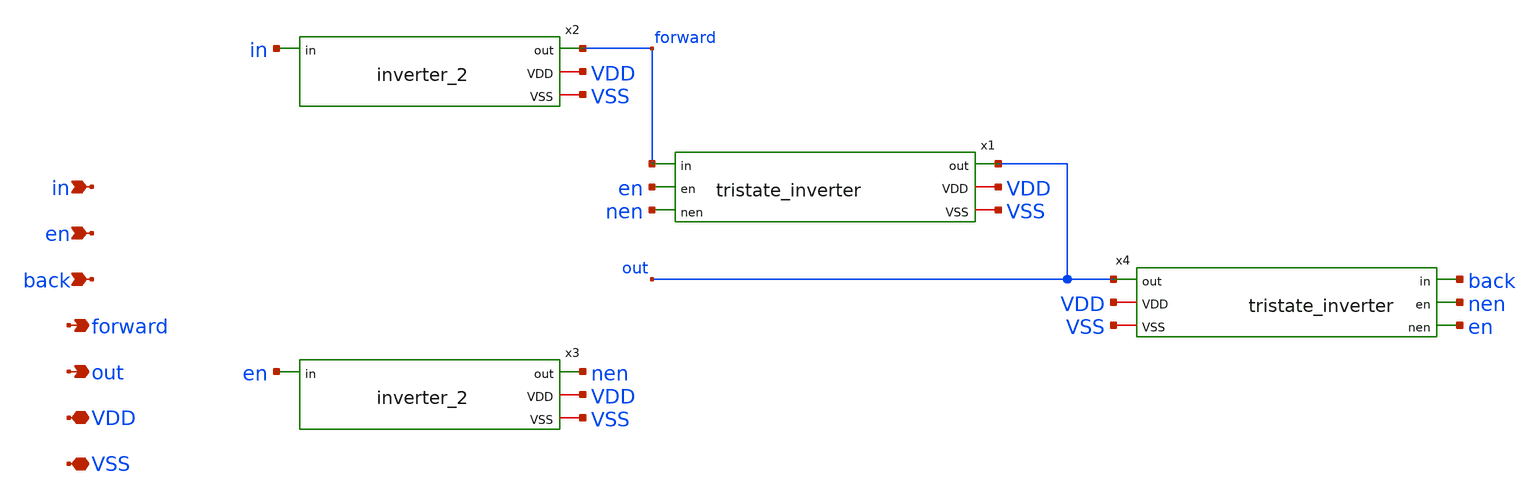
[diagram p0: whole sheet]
** sch_path: xschem/variable_delay_unit.sch
**.subckt variable_delay_unit VDD in out VSS en back forward
*.iopin VDD
*.ipin in
*.opin out
*.iopin VSS
*.ipin en
*.ipin back
*.opin forward
x1 forward en nen out VDD VSS tristate_inverter
x2 in forward VDD VSS inverter_2
x3 en nen VDD VSS inverter_2
x4 back nen en out VDD VSS tristate_inverter
**.ends

* expanding   symbol:  tristate_inverter.sym # of pins=6
** sym_path: xschem/tristate_inverter.sym
** sch_path: xschem/tristate_inverter.sch
.subckt tristate_inverter in en nen out VDD VSS
*.iopin VDD
*.ipin in
*.opin out
*.iopin VSS
*.ipin en
*.ipin nen
XM5 out in net2 VDD sky130_fd_pr__pfet_01v8 L=0.15 W=3 nf=1 ad='int((nf+1)/2) * W/nf * 0.29' as='int((nf+2)/2) * W/nf * 0.29'
+ pd='2*int((nf+1)/2) * (W/nf + 0.29)' ps='2*int((nf+2)/2) * (W/nf + 0.29)' nrd='0.29 / W' nrs='0.29 / W'
+ sa=0 sb=0 sd=0 mult=1 m=1
XM7 out in net1 VSS sky130_fd_pr__nfet_01v8 L=0.15 W=1 nf=1 ad='int((nf+1)/2) * W/nf * 0.29' as='int((nf+2)/2) * W/nf * 0.29'
+ pd='2*int((nf+1)/2) * (W/nf + 0.29)' ps='2*int((nf+2)/2) * (W/nf + 0.29)' nrd='0.29 / W' nrs='0.29 / W'
+ sa=0 sb=0 sd=0 mult=1 m=1
XM1 net2 nen VDD VDD sky130_fd_pr__pfet_01v8 L=0.15 W=9 nf=1 ad='int((nf+1)/2) * W/nf * 0.29' as='int((nf+2)/2) * W/nf * 0.29'
+ pd='2*int((nf+1)/2) * (W/nf + 0.29)' ps='2*int((nf+2)/2) * (W/nf + 0.29)' nrd='0.29 / W' nrs='0.29 / W'
+ sa=0 sb=0 sd=0 mult=1 m=1
XM2 net1 en VSS VSS sky130_fd_pr__nfet_01v8 L=0.15 W=3 nf=1 ad='int((nf+1)/2) * W/nf * 0.29' as='int((nf+2)/2) * W/nf * 0.29'
+ pd='2*int((nf+1)/2) * (W/nf + 0.29)' ps='2*int((nf+2)/2) * (W/nf + 0.29)' nrd='0.29 / W' nrs='0.29 / W'
+ sa=0 sb=0 sd=0 mult=1 m=1
.ends


* expanding   symbol:  inverter_2.sym # of pins=4
** sym_path: xschem/inverter_2.sym
** sch_path: xschem/inverter_2.sch
.subckt inverter_2 in out VDD VSS
*.iopin VDD
*.ipin in
*.opin out
*.iopin VSS
XM1 out in VDD VDD sky130_fd_pr__pfet_01v8 L=0.15 W=3 nf=1 ad='int((nf+1)/2) * W/nf * 0.29' as='int((nf+2)/2) * W/nf * 0.29'
+ pd='2*int((nf+1)/2) * (W/nf + 0.29)' ps='2*int((nf+2)/2) * (W/nf + 0.29)' nrd='0.29 / W' nrs='0.29 / W'
+ sa=0 sb=0 sd=0 mult=1 m=1
XM2 out in VSS VSS sky130_fd_pr__nfet_01v8 L=0.15 W=1 nf=1 ad='int((nf+1)/2) * W/nf * 0.29' as='int((nf+2)/2) * W/nf * 0.29'
+ pd='2*int((nf+1)/2) * (W/nf + 0.29)' ps='2*int((nf+2)/2) * (W/nf + 0.29)' nrd='0.29 / W' nrs='0.29 / W'
+ sa=0 sb=0 sd=0 mult=1 m=1
.ends

.end
